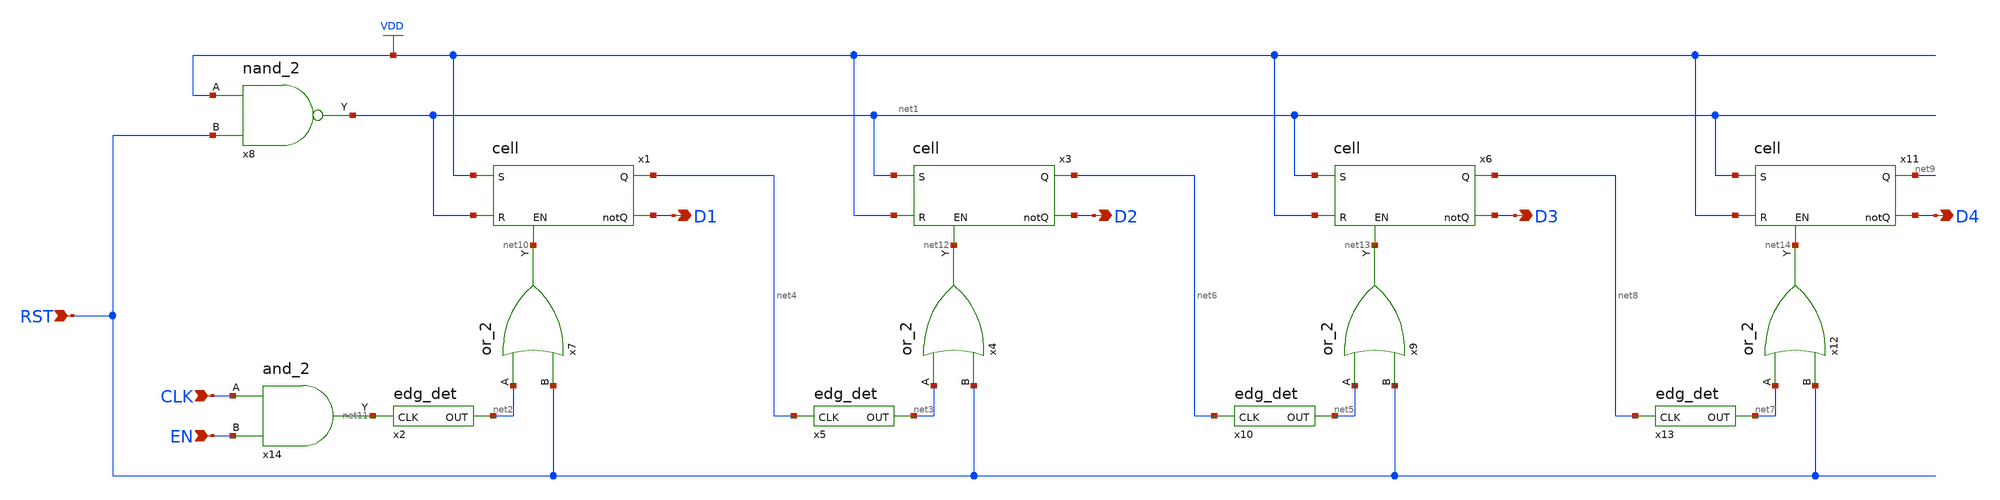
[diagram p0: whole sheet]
** sch_path: Circuiti/counter/counter.sch
**.subckt counter RST CLK D1 D2 D3 D4 EN
*.ipin RST
*.ipin CLK
*.opin D1
*.opin D2
*.opin D3
*.opin D4
*.ipin EN
x1 net4 VDD net1 D1 net10 cell
x7 net2 net10 RST or_2
x8 VDD net1 RST nand_2
x2 net2 net11 edg_det
x3 net6 net1 VDD D2 net12 cell
x4 net3 net12 RST or_2
x5 net3 net4 edg_det
x6 net8 net1 VDD D3 net13 cell
x9 net5 net13 RST or_2
x10 net5 net6 edg_det
x11 net9 net1 VDD D4 net14 cell
x12 net7 net14 RST or_2
x13 net7 net8 edg_det
x14 CLK net11 EN and_2
**.ends
.GLOBAL VDD
.end
